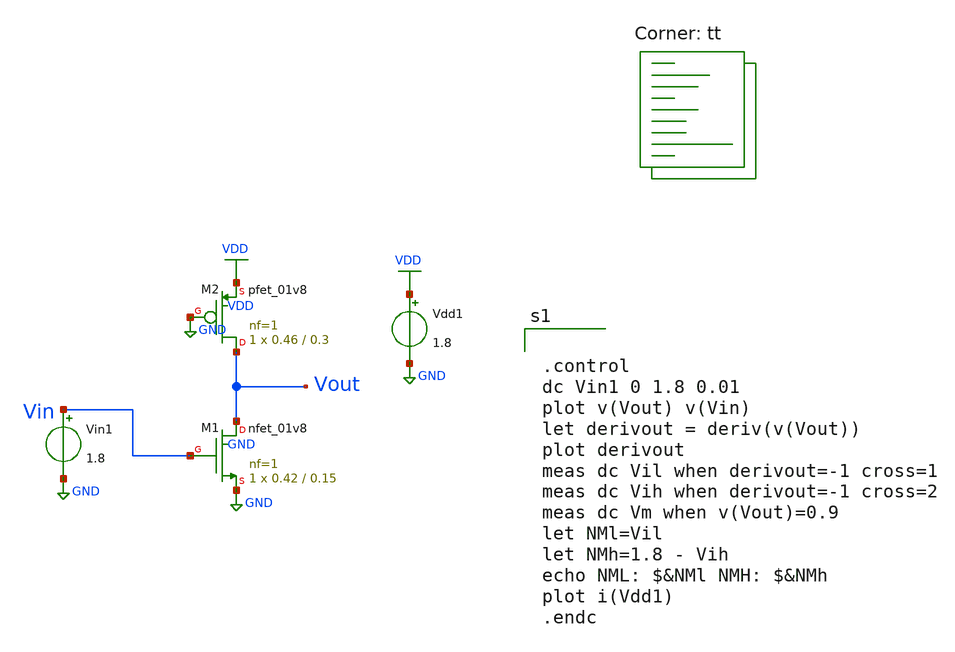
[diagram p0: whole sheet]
** sch_path: Tutorial_2/NoiseMargine_extraction.sch
**.subckt NoiseMargine_extraction
XM1 Vout Vin GND GND sky130_fd_pr__nfet_01v8 L=0.15 W=0.42 nf=1 ad='int((nf+1)/2) * W/nf * 0.29' as='int((nf+2)/2) * W/nf * 0.29'
+ pd='2*int((nf+1)/2) * (W/nf + 0.29)' ps='2*int((nf+2)/2) * (W/nf + 0.29)' nrd='0.29 / W' nrs='0.29 / W'
+ sa=0 sb=0 sd=0 mult=1 m=1
XM2 Vout GND VDD VDD sky130_fd_pr__pfet_01v8 L=0.3 W=0.46 nf=1 ad='int((nf+1)/2) * W/nf * 0.29' as='int((nf+2)/2) * W/nf * 0.29'
+ pd='2*int((nf+1)/2) * (W/nf + 0.29)' ps='2*int((nf+2)/2) * (W/nf + 0.29)' nrd='0.29 / W' nrs='0.29 / W'
+ sa=0 sb=0 sd=0 mult=1 m=1
Vdd1 VDD GND 1.8
Vin1 Vin GND 1.8
**** begin user architecture code


.control
dc Vin1 0 1.8 0.01
plot v(Vout) v(Vin)
let derivout = deriv(v(Vout))
plot derivout
meas dc Vil when derivout=-1 cross=1
meas dc Vih when derivout=-1 cross=2
meas dc Vm when v(Vout)=0.9
let NMl=Vil
let NMh=1.8 - Vih
echo NML: $&NMl NMH: $&NMh
plot i(Vdd1)
.endc


.lib $::SKYWATER_MODELS/sky130.lib.spice tt
**** end user architecture code
**.ends
.GLOBAL GND
.GLOBAL VDD
.end
